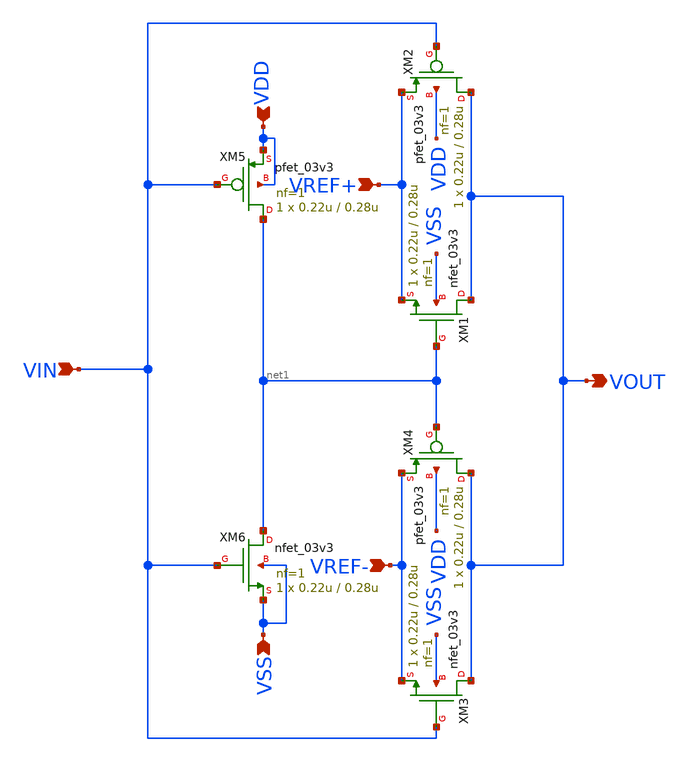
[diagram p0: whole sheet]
** sch_path: src/schematics/dac1bit/DAC_1_BIT.sch
**.subckt DAC_1_BIT VIN VREF+ VREF- VOUT VDD VSS
*.ipin VIN
*.ipin VREF+
*.ipin VREF-
*.opin VOUT
*.ipin VDD
*.ipin VSS
XM1 VOUT net1 VREF+ VSS nfet_03v3 L=0.28u W=0.22u nf=1 ad='int((nf+1)/2) * W/nf * 0.18u' as='int((nf+2)/2) * W/nf * 0.18u'
+ pd='2*int((nf+1)/2) * (W/nf + 0.18u)' ps='2*int((nf+2)/2) * (W/nf + 0.18u)' nrd='0.18u / W' nrs='0.18u / W'
+ sa=0 sb=0 sd=0 m=1
XM2 VOUT VIN VREF+ VDD pfet_03v3 L=0.28u W=0.22u nf=1 ad='int((nf+1)/2) * W/nf * 0.18u' as='int((nf+2)/2) * W/nf * 0.18u'
+ pd='2*int((nf+1)/2) * (W/nf + 0.18u)' ps='2*int((nf+2)/2) * (W/nf + 0.18u)' nrd='0.18u / W' nrs='0.18u / W'
+ sa=0 sb=0 sd=0 m=1
XM3 VOUT VIN VREF- VSS nfet_03v3 L=0.28u W=0.22u nf=1 ad='int((nf+1)/2) * W/nf * 0.18u' as='int((nf+2)/2) * W/nf * 0.18u'
+ pd='2*int((nf+1)/2) * (W/nf + 0.18u)' ps='2*int((nf+2)/2) * (W/nf + 0.18u)' nrd='0.18u / W' nrs='0.18u / W'
+ sa=0 sb=0 sd=0 m=1
XM4 VOUT net1 VREF- VDD pfet_03v3 L=0.28u W=0.22u nf=1 ad='int((nf+1)/2) * W/nf * 0.18u' as='int((nf+2)/2) * W/nf * 0.18u'
+ pd='2*int((nf+1)/2) * (W/nf + 0.18u)' ps='2*int((nf+2)/2) * (W/nf + 0.18u)' nrd='0.18u / W' nrs='0.18u / W'
+ sa=0 sb=0 sd=0 m=1
XM5 net1 VIN VDD VDD pfet_03v3 L=0.28u W=0.22u nf=1 ad='int((nf+1)/2) * W/nf * 0.18u' as='int((nf+2)/2) * W/nf * 0.18u'
+ pd='2*int((nf+1)/2) * (W/nf + 0.18u)' ps='2*int((nf+2)/2) * (W/nf + 0.18u)' nrd='0.18u / W' nrs='0.18u / W'
+ sa=0 sb=0 sd=0 m=1
XM6 net1 VIN VSS VSS nfet_03v3 L=0.28u W=0.22u nf=1 ad='int((nf+1)/2) * W/nf * 0.18u' as='int((nf+2)/2) * W/nf * 0.18u'
+ pd='2*int((nf+1)/2) * (W/nf + 0.18u)' ps='2*int((nf+2)/2) * (W/nf + 0.18u)' nrd='0.18u / W' nrs='0.18u / W'
+ sa=0 sb=0 sd=0 m=1
**.ends
.end
